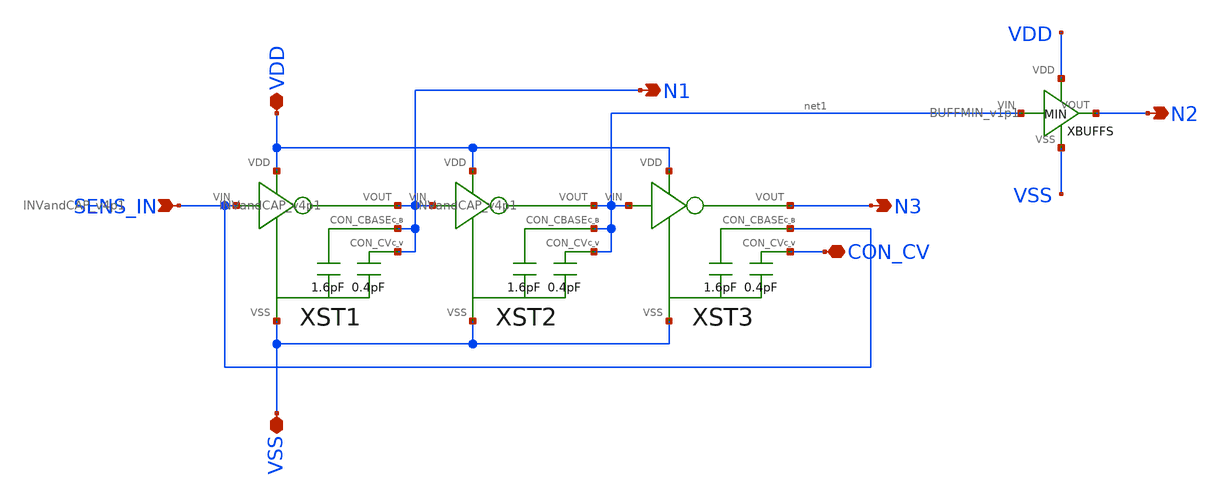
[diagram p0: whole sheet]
** sch_path: samples/cace-tests/SDC/xschem/OSC_v7p1.sch
**.subckt OSC_v7p1 SENS_IN VDD VSS N1 N2 CON_CV N3
*.ipin SENS_IN
*.iopin VDD
*.iopin VSS
*.opin N1
*.opin N2
*.iopin CON_CV
*.opin N3
XST1 SENS_IN VDD VSS N1 N1 N1 INVandCAP_v4p1
XST2 N1 VDD VSS net1 net1 net1 INVandCAP_v4p1
XST3 net1 VDD VSS N3 CON_CV SENS_IN INVandCAP_v4p1
XBUFFS net1 N2 VDD VSS BUFFMIN_v1p1
**.ends

* expanding   symbol:  INVandCAP_v4p1.sym # of pins=6
** sym_path: samples/cace-tests/SDC/xschem/INVandCAP_v4p1.sym
** sch_path: samples/cace-tests/SDC/xschem/INVandCAP_v4p1.sch
.subckt INVandCAP_v4p1 VIN VDD VSS VOUT CON_CV CON_CBASE
*.ipin VIN
*.iopin VDD
*.iopin VSS
*.opin VOUT
*.iopin CON_CV
*.iopin CON_CBASE
XINV_OSC VIN VOUT VDD VSS INV_v1p1
XCN CON_CV CON_CBASE VSS CAPOSC_v3p1
.ends


* expanding   symbol:  BUFFMIN_v1p1.sym # of pins=4
** sym_path: samples/cace-tests/SDC/xschem/BUFFMIN_v1p1.sym
** sch_path: samples/cace-tests/SDC/xschem/BUFFMIN_v1p1.sch
.subckt BUFFMIN_v1p1 VIN VOUT VDD VSS
*.iopin VDD
*.iopin VSS
*.ipin VIN
*.opin VOUT
X1 VIN net1 VDD VSS INVMIN_v1p1
X2 net1 VOUT VDD VSS INVMIN_v1p1
.ends


* expanding   symbol:  INV_v1p1.sym # of pins=4
** sym_path: samples/cace-tests/SDC/xschem/INV_v1p1.sym
** sch_path: samples/cace-tests/SDC/xschem/INV_v1p1.sch
.subckt INV_v1p1 VIN VOUT VDD VSS
*.ipin VIN
*.iopin VDD
*.iopin VSS
*.opin VOUT
XM1 VOUT VIN VSS VSS sky130_fd_pr__nfet_01v8 L=0.15 W=2 nf=2 ad='int((nf+1)/2) * W/nf * 0.29' as='int((nf+2)/2) * W/nf * 0.29'
+ pd='2*int((nf+1)/2) * (W/nf + 0.29)' ps='2*int((nf+2)/2) * (W/nf + 0.29)' nrd='0.29 / W' nrs='0.29 / W'
+ sa=0 sb=0 sd=0 mult=1 m=1
XM2 VOUT VIN VDD VDD sky130_fd_pr__pfet_01v8 L=0.15 W=6 nf=6 ad='int((nf+1)/2) * W/nf * 0.29' as='int((nf+2)/2) * W/nf * 0.29'
+ pd='2*int((nf+1)/2) * (W/nf + 0.29)' ps='2*int((nf+2)/2) * (W/nf + 0.29)' nrd='0.29 / W' nrs='0.29 / W'
+ sa=0 sb=0 sd=0 mult=1 m=1
.ends


* expanding   symbol:  CAPOSC_v3p1.sym # of pins=3
** sym_path: samples/cace-tests/SDC/xschem/CAPOSC_v3p1.sym
** sch_path: samples/cace-tests/SDC/xschem/CAPOSC_v3p1.sch
.subckt CAPOSC_v3p1 TOP_V TOP_B BOT
*.iopin TOP_V
*.iopin TOP_B
*.iopin BOT
XC1_V TOP_V BOT sky130_fd_pr__cap_mim_m3_1 W=10 L=10 MF=1 m=1
XC2_V TOP_V BOT sky130_fd_pr__cap_mim_m3_2 W=10 L=10 MF=1 m=1
XC1_B TOP_B BOT sky130_fd_pr__cap_mim_m3_1 W=10 L=10 MF=1 m=1
XC2_B TOP_B BOT sky130_fd_pr__cap_mim_m3_2 W=10 L=10 MF=1 m=1
XC5_B TOP_B BOT sky130_fd_pr__cap_mim_m3_1 W=10 L=10 MF=1 m=1
XC6_B TOP_B BOT sky130_fd_pr__cap_mim_m3_2 W=10 L=10 MF=1 m=1
XC3_B TOP_B BOT sky130_fd_pr__cap_mim_m3_1 W=10 L=10 MF=1 m=1
XC4_B TOP_B BOT sky130_fd_pr__cap_mim_m3_2 W=10 L=10 MF=1 m=1
XC7_B TOP_B BOT sky130_fd_pr__cap_mim_m3_1 W=10 L=10 MF=1 m=1
XC8_B TOP_B BOT sky130_fd_pr__cap_mim_m3_2 W=10 L=10 MF=1 m=1
XC9_B TOP_B BOT sky130_fd_pr__cap_mim_m3_1 W=10 L=10 MF=1 m=1
XC10_B TOP_B BOT sky130_fd_pr__cap_mim_m3_2 W=10 L=10 MF=1 m=1
.ends


* expanding   symbol:  INVMIN_v1p1.sym # of pins=4
** sym_path: samples/cace-tests/SDC/xschem/INVMIN_v1p1.sym
** sch_path: samples/cace-tests/SDC/xschem/INVMIN_v1p1.sch
.subckt INVMIN_v1p1 VIN VOUT VDD VSS
*.ipin VIN
*.iopin VDD
*.iopin VSS
*.opin VOUT
XM1 VOUT VIN VSS VSS sky130_fd_pr__nfet_01v8 L=0.15 W=1 nf=1 ad='int((nf+1)/2) * W/nf * 0.29' as='int((nf+2)/2) * W/nf * 0.29'
+ pd='2*int((nf+1)/2) * (W/nf + 0.29)' ps='2*int((nf+2)/2) * (W/nf + 0.29)' nrd='0.29 / W' nrs='0.29 / W'
+ sa=0 sb=0 sd=0 mult=1 m=1
XM2 VOUT VIN VDD VDD sky130_fd_pr__pfet_01v8 L=0.15 W=1 nf=1 ad='int((nf+1)/2) * W/nf * 0.29' as='int((nf+2)/2) * W/nf * 0.29'
+ pd='2*int((nf+1)/2) * (W/nf + 0.29)' ps='2*int((nf+2)/2) * (W/nf + 0.29)' nrd='0.29 / W' nrs='0.29 / W'
+ sa=0 sb=0 sd=0 mult=1 m=1
.ends

.end
